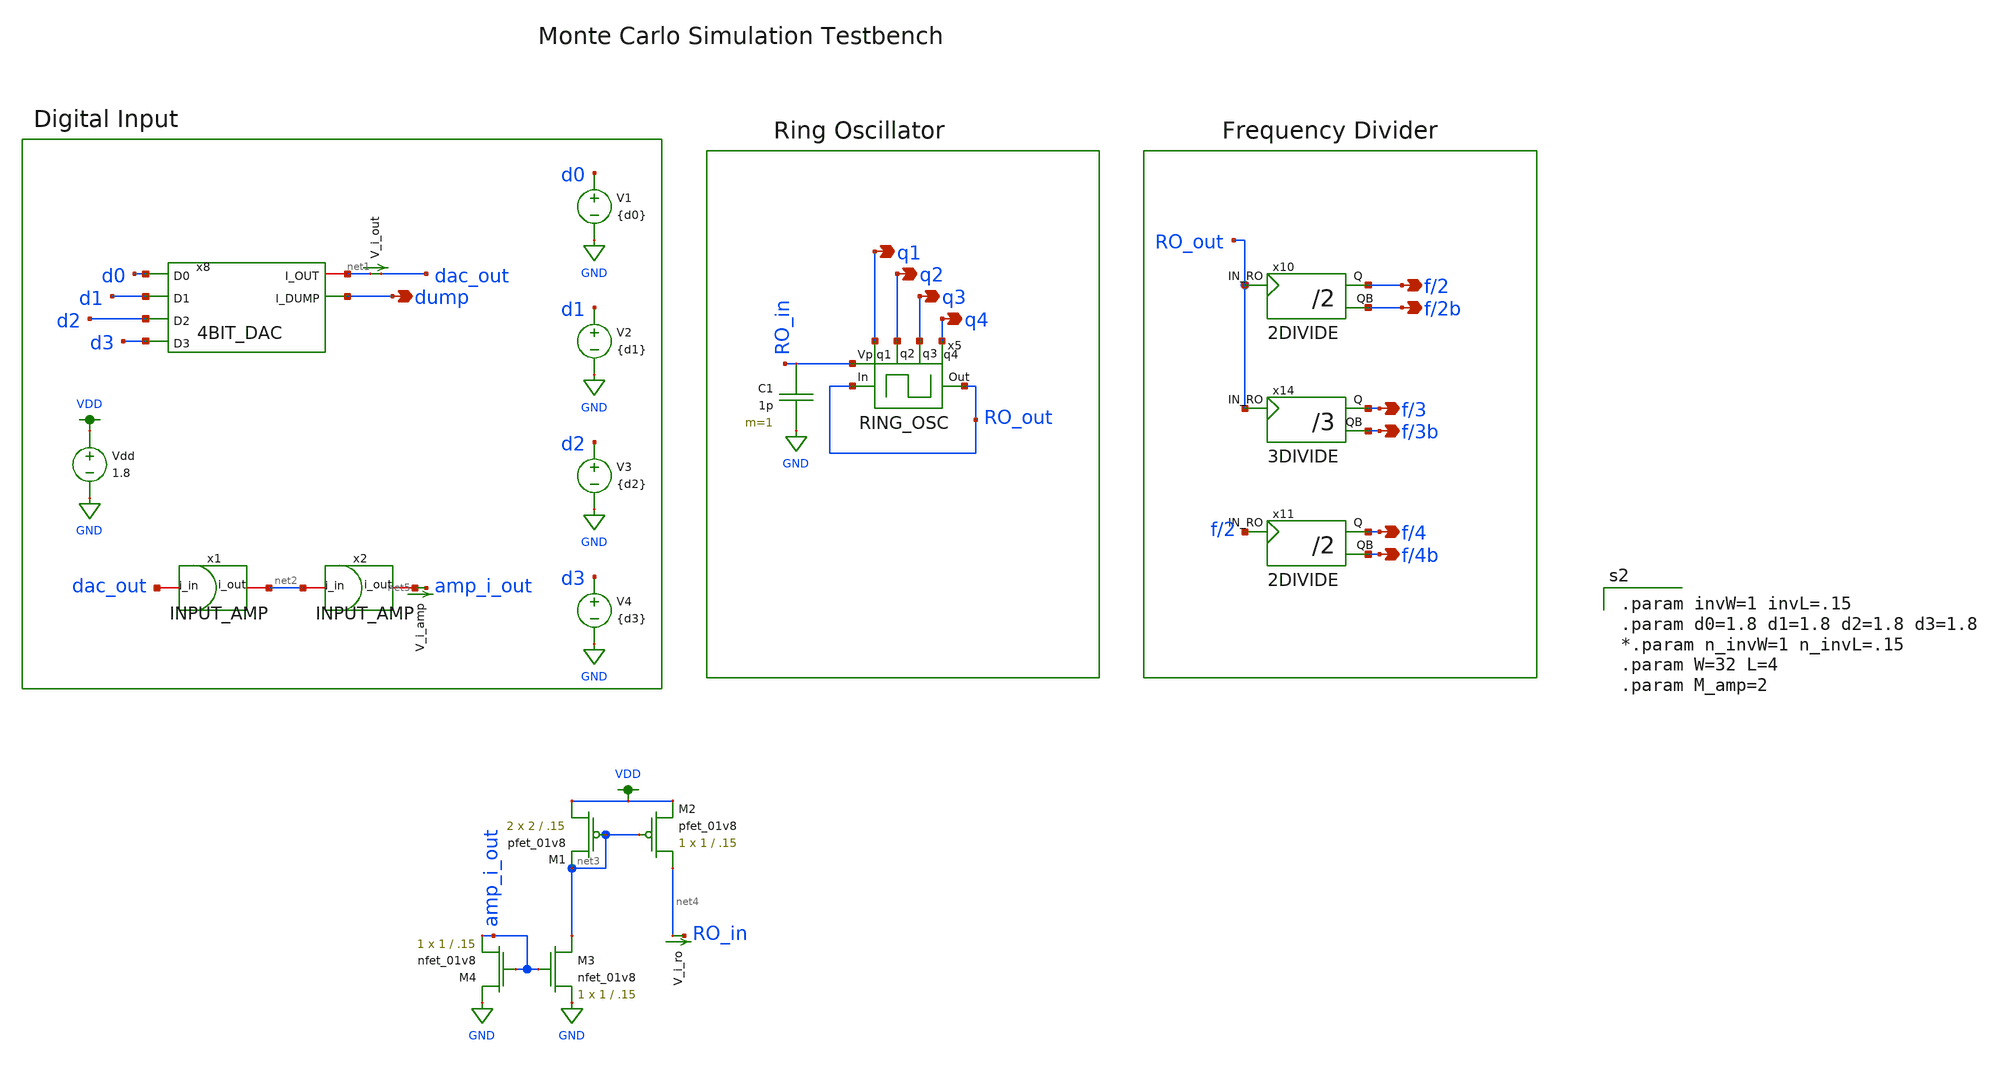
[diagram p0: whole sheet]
** sch_path: schemas/temperature_testbench.sch
**.subckt temperature_testbench dump f/2 f/4 f/3 f/3b f/4b f/2b q1 q2 q3 q4
*.opin dump
*.opin f/2
*.opin f/4
*.opin f/3
*.opin f/3b
*.opin f/4b
*.opin f/2b
*.opin q1
*.opin q2
*.opin q3
*.opin q4
x8 net1 dump d1 d0 d2 d3 4BIT_DAC
x10 f/2 f/2b RO_out 2DIVIDE
x11 f/4 f/4b f/2 2DIVIDE
V_i_out net1 dac_out 0
.save i(v_i_out)
x14 f/3 f/3b RO_out 3DIVIDE
V2 d1 GND {d1}
V1 d0 GND {d0}
V3 d2 GND {d2}
V4 d3 GND {d3}
x1 dac_out net2 INPUT_AMP
x2 net2 net5 INPUT_AMP
x5 q4 q1 q2 q3 RO_out RO_out RO_in RING_OSC
V_i_ro net4 RO_in 0
.save i(v_i_ro)
Vdd VDD GND 1.8
XM1 VDD net3 net3 VDD sky130_fd_pr__pfet_01v8 L=.15 W=2 nf=1 ad='int((nf+1)/2) * W/nf * 0.29' as='int((nf+2)/2) * W/nf * 0.29'
+ pd='2*int((nf+1)/2) * (W/nf + 0.29)' ps='2*int((nf+2)/2) * (W/nf + 0.29)' nrd='0.29 / W' nrs='0.29 / W'
+ sa=0 sb=0 sd=0 mult=2 m=2
XM2 net4 net3 VDD VDD sky130_fd_pr__pfet_01v8 L=.15 W=1 nf=1 ad='int((nf+1)/2) * W/nf * 0.29' as='int((nf+2)/2) * W/nf * 0.29'
+ pd='2*int((nf+1)/2) * (W/nf + 0.29)' ps='2*int((nf+2)/2) * (W/nf + 0.29)' nrd='0.29 / W' nrs='0.29 / W'
+ sa=0 sb=0 sd=0 mult=1 m=1
XM3 net3 amp_i_out GND GND sky130_fd_pr__nfet_01v8 L=.15 W=1 nf=1 ad='int((nf+1)/2) * W/nf * 0.29' as='int((nf+2)/2) * W/nf * 0.29'
+ pd='2*int((nf+1)/2) * (W/nf + 0.29)' ps='2*int((nf+2)/2) * (W/nf + 0.29)' nrd='0.29 / W' nrs='0.29 / W'
+ sa=0 sb=0 sd=0 mult=1 m=1
XM4 GND amp_i_out amp_i_out GND sky130_fd_pr__nfet_01v8 L=.15 W=1 nf=1 ad='int((nf+1)/2) * W/nf * 0.29'
+ as='int((nf+2)/2) * W/nf * 0.29' pd='2*int((nf+1)/2) * (W/nf + 0.29)' ps='2*int((nf+2)/2) * (W/nf + 0.29)'
+ nrd='0.29 / W' nrs='0.29 / W' sa=0 sb=0 sd=0 mult=1 m=1
C1 RO_in GND 1p m=1
V_i_amp net5 amp_i_out 0
.save i(v_i_amp)
**** begin user architecture code

.option wnflag=1
.lib ~/skywater/skywater-pdk/libraries/sky130_fd_pr_ngspice/latest/models/sky130.lib.spice tt




.tran 0.01n 100n
.save i(V_i_out) i(V_i_amp) i(V_i_ro) v(RO_out) v(V_out) v(f/2) v(f/4) v(f/3) v(q1) v(q2) v(q3) v(q4)

.control
foreach .temp 0 10 20 30 40 50 60 70 80
run

plot i(V_i_amp) i(V_i_out) i(V_i_ro)
plot v(q1) v(q2) v(q3) v(q4)
end

*plot i(V_i_amp) i(V_i_out) i(V_i_ro)
*plot v(q1) v(q2) v(q3) v(q4)
.endc



.param invW=1 invL=.15
.param d0=1.8 d1=1.8 d2=1.8 d3=1.8
*.param n_invW=1 n_invL=.15
.param W=32 L=4
.param M_amp=2


**** end user architecture code
**.ends
.GLOBAL GND
.GLOBAL VDD
.end
